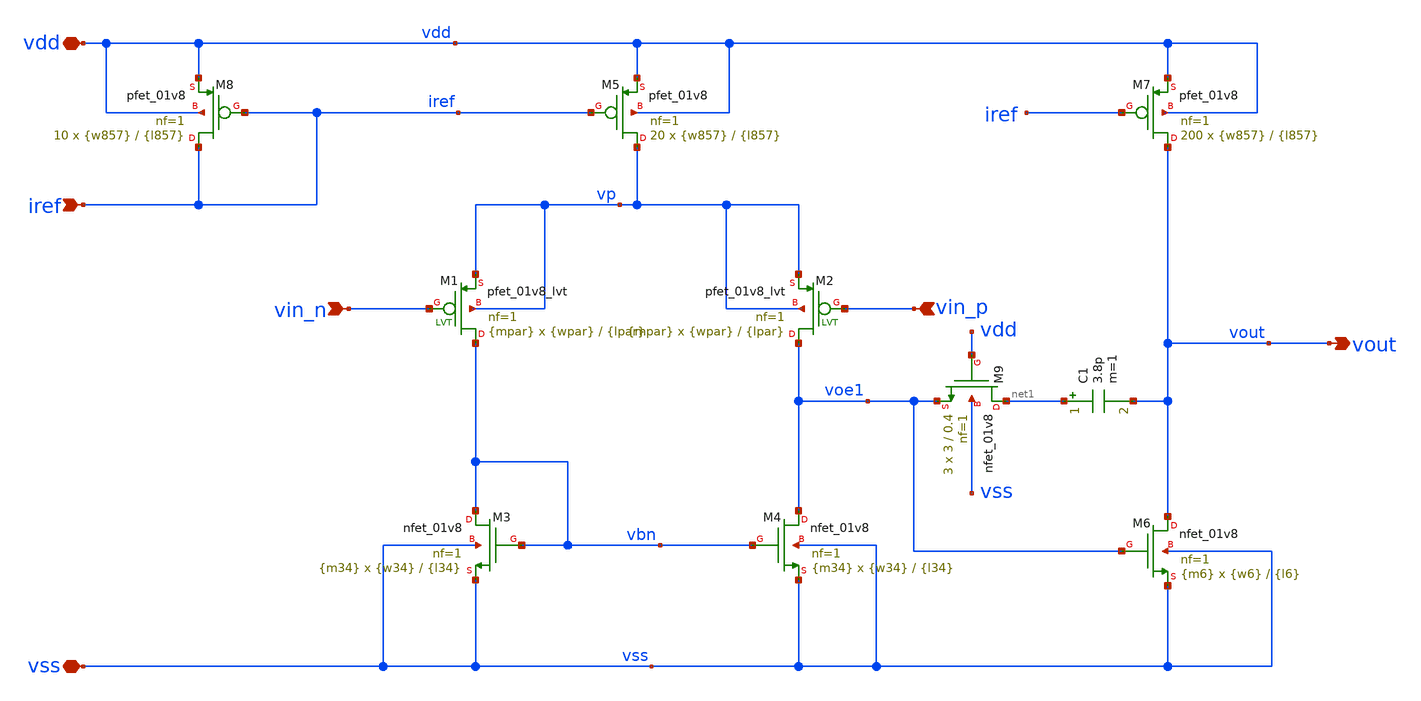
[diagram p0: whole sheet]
** sch_path: opamp.sch
**.subckt opamp vdd vss vin_n vin_p iref vout
*.iopin vdd
*.iopin vss
*.ipin vin_n
*.ipin vin_p
*.ipin iref
*.opin vout
XM3 vbn vbn vss vss sky130_fd_pr__nfet_01v8 L={l34} W={w34} nf=1 ad='W * 0.29' as='W * 0.29' pd='2 * (W + 0.29)'
+ ps='2 * (W + 0.29)' nrd='0.29 / W' nrs='0.29 / W' sa=0 sb=0 sd=0 mult={m34} m={m34}
XM4 voe1 vbn vss vss sky130_fd_pr__nfet_01v8 L={l34} W={w34} nf=1 ad='W * 0.29' as='W * 0.29' pd='2 * (W + 0.29)'
+ ps='2 * (W + 0.29)' nrd='0.29 / W' nrs='0.29 / W' sa=0 sb=0 sd=0 mult={m34} m={m34}
XM5 vp iref vdd vdd sky130_fd_pr__pfet_01v8 L={l857} W={w857} nf=1 ad='W * 0.29' as='W * 0.29' pd='2 * (W + 0.29)'
+ ps='2 * (W + 0.29)' nrd='0.29 / W' nrs='0.29 / W' sa=0 sb=0 sd=0 mult=20 m=20
XM7 vout iref vdd vdd sky130_fd_pr__pfet_01v8 L={l857} W={w857} nf=1 ad='W * 0.29' as='W * 0.29' pd='2 * (W + 0.29)'
+ ps='2 * (W + 0.29)' nrd='0.29 / W' nrs='0.29 / W' sa=0 sb=0 sd=0 mult=200 m=200
XM8 iref iref vdd vdd sky130_fd_pr__pfet_01v8 L={l857} W={w857} nf=1 ad='W * 0.29' as='W * 0.29' pd='2 * (W + 0.29)'
+ ps='2 * (W + 0.29)' nrd='0.29 / W' nrs='0.29 / W' sa=0 sb=0 sd=0 mult=10 m=10
XM9 net1 vdd voe1 vss sky130_fd_pr__nfet_01v8 L=0.4 W=3 nf=1 ad='W * 0.29' as='W * 0.29' pd='2 * (W + 0.29)'
+ ps='2 * (W + 0.29)' nrd='0.29 / W' nrs='0.29 / W' sa=0 sb=0 sd=0 mult=3 m=3
XM6 vout voe1 vss vss sky130_fd_pr__nfet_01v8 L={l6} W={w6} nf=1 ad='W * 0.29' as='W * 0.29' pd='2 * (W + 0.29)'
+ ps='2 * (W + 0.29)' nrd='0.29 / W' nrs='0.29 / W' sa=0 sb=0 sd=0 mult={m6} m={m6}
XM1 vbn vin_n vp vp sky130_fd_pr__pfet_01v8_lvt L={lpar} W={wpar} nf=1 ad='int((nf+1)/2) * W/nf * 0.29'
+ as='int((nf+2)/2) * W/nf * 0.29' pd='2*int((nf+1)/2) * (W/nf + 0.29)' ps='2*int((nf+2)/2) * (W/nf + 0.29)'
+ nrd='0.29 / W' nrs='0.29 / W' sa=0 sb=0 sd=0 mult={mpar} m={mpar}
XM2 voe1 vin_p vp vp sky130_fd_pr__pfet_01v8_lvt L={lpar} W={wpar} nf=1 ad='int((nf+1)/2) * W/nf * 0.29'
+ as='int((nf+2)/2) * W/nf * 0.29' pd='2*int((nf+1)/2) * (W/nf + 0.29)' ps='2*int((nf+2)/2) * (W/nf + 0.29)'
+ nrd='0.29 / W' nrs='0.29 / W' sa=0 sb=0 sd=0 mult={mpar} m={mpar}
C1 net1 vout 3.8p m=1
**.ends
.end
